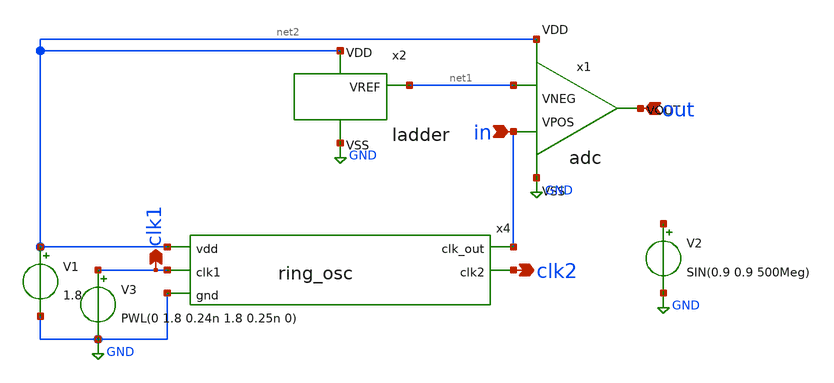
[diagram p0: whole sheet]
** sch_path: week4/xschem/adc/adc_tb.sch
**.subckt adc_tb in out clk1 clk2
*.ipin in
*.ipin out
*.opin clk1
*.opin clk2
x1 out net2 net1 in GND adc
x2 net1 net2 GND ladder
x4 net2 in clk1 clk2 GND ring_osc
V1 net2 GND 1.8
V3 clk1 GND PWL(0 1.8 0.24n 1.8 0.25n 0)
V2 net3 GND SIN(0.9 0.9 500Meg)
**** begin user architecture code


.lib /usr/local/share/pdk/sky130A/libs.tech/ngspice/sky130.lib.spice tt
.control
	tran 0.01n 4n
	plot v(in) v(out)
.endc
.save all


**** end user architecture code
**.ends

* expanding   symbol:  adc.sym # of pins=5
** sym_path: week4/xschem/adc/adc.sym
** sch_path: week4/xschem/adc/adc.sch
.subckt adc VOUT VDD VNEG VPOS VSS
*.ipin VDD
*.opin VOUT
*.ipin VSS
*.ipin VNEG
*.ipin VPOS
XM1 VREF VREF VSS VSS sky130_fd_pr__nfet_01v8 L=0.15 W=1 nf=1 ad='int((nf+1)/2) * W/nf * 0.29' as='int((nf+2)/2) * W/nf * 0.29'
+ pd='2*int((nf+1)/2) * (W/nf + 0.29)' ps='2*int((nf+2)/2) * (W/nf + 0.29)' nrd='0.29 / W' nrs='0.29 / W'
+ sa=0 sb=0 sd=0 mult=1 m=1
XM2 VREF VREF VDD VDD sky130_fd_pr__pfet_01v8 L=0.15 W=1 nf=1 ad='int((nf+1)/2) * W/nf * 0.29' as='int((nf+2)/2) * W/nf * 0.29'
+ pd='2*int((nf+1)/2) * (W/nf + 0.29)' ps='2*int((nf+2)/2) * (W/nf + 0.29)' nrd='0.29 / W' nrs='0.29 / W'
+ sa=0 sb=0 sd=0 mult=1 m=1
XM3 net1 VREF VDD VDD sky130_fd_pr__pfet_01v8 L=0.15 W=3 nf=1 ad='int((nf+1)/2) * W/nf * 0.29' as='int((nf+2)/2) * W/nf * 0.29'
+ pd='2*int((nf+1)/2) * (W/nf + 0.29)' ps='2*int((nf+2)/2) * (W/nf + 0.29)' nrd='0.29 / W' nrs='0.29 / W'
+ sa=0 sb=0 sd=0 mult=1 m=1
XM4 net2 VNEG net1 VDD sky130_fd_pr__pfet_01v8 L=0.15 W=3 nf=1 ad='int((nf+1)/2) * W/nf * 0.29' as='int((nf+2)/2) * W/nf * 0.29'
+ pd='2*int((nf+1)/2) * (W/nf + 0.29)' ps='2*int((nf+2)/2) * (W/nf + 0.29)' nrd='0.29 / W' nrs='0.29 / W'
+ sa=0 sb=0 sd=0 mult=1 m=1
XM5 DIFF VPOS net1 VDD sky130_fd_pr__pfet_01v8 L=0.15 W=3 nf=1 ad='int((nf+1)/2) * W/nf * 0.29' as='int((nf+2)/2) * W/nf * 0.29'
+ pd='2*int((nf+1)/2) * (W/nf + 0.29)' ps='2*int((nf+2)/2) * (W/nf + 0.29)' nrd='0.29 / W' nrs='0.29 / W'
+ sa=0 sb=0 sd=0 mult=1 m=1
XM6 net2 net2 VSS VSS sky130_fd_pr__nfet_01v8 L=0.15 W=1 nf=1 ad='int((nf+1)/2) * W/nf * 0.29' as='int((nf+2)/2) * W/nf * 0.29'
+ pd='2*int((nf+1)/2) * (W/nf + 0.29)' ps='2*int((nf+2)/2) * (W/nf + 0.29)' nrd='0.29 / W' nrs='0.29 / W'
+ sa=0 sb=0 sd=0 mult=1 m=1
XM7 DIFF net2 VSS VSS sky130_fd_pr__nfet_01v8 L=0.15 W=1 nf=1 ad='int((nf+1)/2) * W/nf * 0.29' as='int((nf+2)/2) * W/nf * 0.29'
+ pd='2*int((nf+1)/2) * (W/nf + 0.29)' ps='2*int((nf+2)/2) * (W/nf + 0.29)' nrd='0.29 / W' nrs='0.29 / W'
+ sa=0 sb=0 sd=0 mult=1 m=1
XM8 VOUT DIFF VSS VSS sky130_fd_pr__nfet_01v8 L=0.15 W=1 nf=1 ad='int((nf+1)/2) * W/nf * 0.29' as='int((nf+2)/2) * W/nf * 0.29'
+ pd='2*int((nf+1)/2) * (W/nf + 0.29)' ps='2*int((nf+2)/2) * (W/nf + 0.29)' nrd='0.29 / W' nrs='0.29 / W'
+ sa=0 sb=0 sd=0 mult=1 m=1
XM9 VOUT VREF VDD VDD sky130_fd_pr__pfet_01v8 L=0.15 W=6 nf=1 ad='int((nf+1)/2) * W/nf * 0.29' as='int((nf+2)/2) * W/nf * 0.29'
+ pd='2*int((nf+1)/2) * (W/nf + 0.29)' ps='2*int((nf+2)/2) * (W/nf + 0.29)' nrd='0.29 / W' nrs='0.29 / W'
+ sa=0 sb=0 sd=0 mult=1 m=1
XM10 VOUT DIFF VOUT VSS sky130_fd_pr__nfet_01v8 L=0.15 W=1 nf=1 ad='int((nf+1)/2) * W/nf * 0.29' as='int((nf+2)/2) * W/nf * 0.29'
+ pd='2*int((nf+1)/2) * (W/nf + 0.29)' ps='2*int((nf+2)/2) * (W/nf + 0.29)' nrd='0.29 / W' nrs='0.29 / W'
+ sa=0 sb=0 sd=0 mult=1 m=1
.ends


* expanding   symbol:  ladder.sym # of pins=3
** sym_path: week4/xschem/adc/ladder.sym
** sch_path: week4/xschem/adc/ladder.sch
.subckt ladder VREF VDD VSS
*.opin VREF
*.ipin VSS
*.ipin VDD
XM1 VREF VREF VSS VSS sky130_fd_pr__nfet_01v8 L=0.15 W=1 nf=1 ad='int((nf+1)/2) * W/nf * 0.29' as='int((nf+2)/2) * W/nf * 0.29'
+ pd='2*int((nf+1)/2) * (W/nf + 0.29)' ps='2*int((nf+2)/2) * (W/nf + 0.29)' nrd='0.29 / W' nrs='0.29 / W'
+ sa=0 sb=0 sd=0 mult=1 m=1
XM2 VREF VREF VDD VDD sky130_fd_pr__pfet_01v8 L=0.15 W=1 nf=1 ad='int((nf+1)/2) * W/nf * 0.29' as='int((nf+2)/2) * W/nf * 0.29'
+ pd='2*int((nf+1)/2) * (W/nf + 0.29)' ps='2*int((nf+2)/2) * (W/nf + 0.29)' nrd='0.29 / W' nrs='0.29 / W'
+ sa=0 sb=0 sd=0 mult=1 m=1
.ends


* expanding   symbol:  ring_osc.sym # of pins=5
** sym_path: week4/xschem/ring/ring_osc.sym
** sch_path: week4/xschem/ring/ring_osc.sch
.subckt ring_osc vdd clk_out clk1 clk2 gnd
*.ipin vdd
*.ipin gnd
*.ipin clk1
*.opin clk_out
*.opin clk2
XM7 vdd clk1 net1 gnd sky130_fd_pr__nfet_01v8 L=0.15 W=1 nf=1 ad='int((nf+1)/2) * W/nf * 0.29' as='int((nf+2)/2) * W/nf * 0.29'
+ pd='2*int((nf+1)/2) * (W/nf + 0.29)' ps='2*int((nf+2)/2) * (W/nf + 0.29)' nrd='0.29 / W' nrs='0.29 / W'
+ sa=0 sb=0 sd=0 mult=1 m=1
XM8 clk2 clk1 gnd gnd sky130_fd_pr__nfet_01v8 L=0.15 W=1 nf=1 ad='int((nf+1)/2) * W/nf * 0.29' as='int((nf+2)/2) * W/nf * 0.29'
+ pd='2*int((nf+1)/2) * (W/nf + 0.29)' ps='2*int((nf+2)/2) * (W/nf + 0.29)' nrd='0.29 / W' nrs='0.29 / W'
+ sa=0 sb=0 sd=0 mult=1 m=1
XM9 clk2 clk1 vdd vdd sky130_fd_pr__pfet_01v8 L=0.15 W=1 nf=1 ad='int((nf+1)/2) * W/nf * 0.29' as='int((nf+2)/2) * W/nf * 0.29'
+ pd='2*int((nf+1)/2) * (W/nf + 0.29)' ps='2*int((nf+2)/2) * (W/nf + 0.29)' nrd='0.29 / W' nrs='0.29 / W'
+ sa=0 sb=0 sd=0 mult=1 m=1
XM10 clk_out clk2 net1 gnd sky130_fd_pr__nfet_01v8 L=0.15 W=1 nf=1 ad='int((nf+1)/2) * W/nf * 0.29' as='int((nf+2)/2) * W/nf * 0.29'
+ pd='2*int((nf+1)/2) * (W/nf + 0.29)' ps='2*int((nf+2)/2) * (W/nf + 0.29)' nrd='0.29 / W' nrs='0.29 / W'
+ sa=0 sb=0 sd=0 mult=1 m=1
x1 vdd gnd clk_out net1 sub_comp
.ends


* expanding   symbol:  sub_comp.sym # of pins=4
** sym_path: week4/xschem/ring/sub_comp.sym
** sch_path: week4/xschem/ring/sub_comp.sch
.subckt sub_comp vdd gnd clkout clkin
*.ipin clkin
*.opin clkout
*.ipin vdd
*.ipin gnd
XM1 net1 clkin gnd gnd sky130_fd_pr__nfet_01v8 L=0.15 W=1 nf=1 ad='int((nf+1)/2) * W/nf * 0.29' as='int((nf+2)/2) * W/nf * 0.29'
+ pd='2*int((nf+1)/2) * (W/nf + 0.29)' ps='2*int((nf+2)/2) * (W/nf + 0.29)' nrd='0.29 / W' nrs='0.29 / W'
+ sa=0 sb=0 sd=0 mult=1 m=1
XM2 net1 clkin vdd vdd sky130_fd_pr__pfet_01v8 L=0.15 W=3 nf=1 ad='int((nf+1)/2) * W/nf * 0.29' as='int((nf+2)/2) * W/nf * 0.29'
+ pd='2*int((nf+1)/2) * (W/nf + 0.29)' ps='2*int((nf+2)/2) * (W/nf + 0.29)' nrd='0.29 / W' nrs='0.29 / W'
+ sa=0 sb=0 sd=0 mult=1 m=1
XM3 net2 net1 gnd gnd sky130_fd_pr__nfet_01v8 L=0.15 W=1 nf=1 ad='int((nf+1)/2) * W/nf * 0.29' as='int((nf+2)/2) * W/nf * 0.29'
+ pd='2*int((nf+1)/2) * (W/nf + 0.29)' ps='2*int((nf+2)/2) * (W/nf + 0.29)' nrd='0.29 / W' nrs='0.29 / W'
+ sa=0 sb=0 sd=0 mult=1 m=1
XM4 net2 net1 vdd vdd sky130_fd_pr__pfet_01v8 L=0.15 W=6 nf=1 ad='int((nf+1)/2) * W/nf * 0.29' as='int((nf+2)/2) * W/nf * 0.29'
+ pd='2*int((nf+1)/2) * (W/nf + 0.29)' ps='2*int((nf+2)/2) * (W/nf + 0.29)' nrd='0.29 / W' nrs='0.29 / W'
+ sa=0 sb=0 sd=0 mult=1 m=1
XM7 clkout net3 gnd gnd sky130_fd_pr__nfet_01v8 L=0.15 W=1 nf=1 ad='int((nf+1)/2) * W/nf * 0.29' as='int((nf+2)/2) * W/nf * 0.29'
+ pd='2*int((nf+1)/2) * (W/nf + 0.29)' ps='2*int((nf+2)/2) * (W/nf + 0.29)' nrd='0.29 / W' nrs='0.29 / W'
+ sa=0 sb=0 sd=0 mult=1 m=1
XM8 clkout net3 vdd vdd sky130_fd_pr__pfet_01v8 L=0.15 W=96 nf=2 ad='int((nf+1)/2) * W/nf * 0.29' as='int((nf+2)/2) * W/nf * 0.29'
+ pd='2*int((nf+1)/2) * (W/nf + 0.29)' ps='2*int((nf+2)/2) * (W/nf + 0.29)' nrd='0.29 / W' nrs='0.29 / W'
+ sa=0 sb=0 sd=0 mult=1 m=1
XM5 net4 net2 gnd gnd sky130_fd_pr__nfet_01v8 L=0.15 W=1 nf=1 ad='int((nf+1)/2) * W/nf * 0.29' as='int((nf+2)/2) * W/nf * 0.29'
+ pd='2*int((nf+1)/2) * (W/nf + 0.29)' ps='2*int((nf+2)/2) * (W/nf + 0.29)' nrd='0.29 / W' nrs='0.29 / W'
+ sa=0 sb=0 sd=0 mult=1 m=1
XM6 net4 net2 vdd vdd sky130_fd_pr__pfet_01v8 L=0.15 W=12 nf=1 ad='int((nf+1)/2) * W/nf * 0.29' as='int((nf+2)/2) * W/nf * 0.29'
+ pd='2*int((nf+1)/2) * (W/nf + 0.29)' ps='2*int((nf+2)/2) * (W/nf + 0.29)' nrd='0.29 / W' nrs='0.29 / W'
+ sa=0 sb=0 sd=0 mult=1 m=1
XM9 net5 net4 gnd gnd sky130_fd_pr__nfet_01v8 L=0.15 W=1 nf=1 ad='int((nf+1)/2) * W/nf * 0.29' as='int((nf+2)/2) * W/nf * 0.29'
+ pd='2*int((nf+1)/2) * (W/nf + 0.29)' ps='2*int((nf+2)/2) * (W/nf + 0.29)' nrd='0.29 / W' nrs='0.29 / W'
+ sa=0 sb=0 sd=0 mult=1 m=1
XM10 net5 net4 vdd vdd sky130_fd_pr__pfet_01v8 L=0.15 W=24 nf=1 ad='int((nf+1)/2) * W/nf * 0.29' as='int((nf+2)/2) * W/nf * 0.29'
+ pd='2*int((nf+1)/2) * (W/nf + 0.29)' ps='2*int((nf+2)/2) * (W/nf + 0.29)' nrd='0.29 / W' nrs='0.29 / W'
+ sa=0 sb=0 sd=0 mult=1 m=1
XM11 net6 net5 gnd gnd sky130_fd_pr__nfet_01v8 L=0.15 W=1 nf=1 ad='int((nf+1)/2) * W/nf * 0.29' as='int((nf+2)/2) * W/nf * 0.29'
+ pd='2*int((nf+1)/2) * (W/nf + 0.29)' ps='2*int((nf+2)/2) * (W/nf + 0.29)' nrd='0.29 / W' nrs='0.29 / W'
+ sa=0 sb=0 sd=0 mult=1 m=1
XM12 net6 net5 vdd vdd sky130_fd_pr__pfet_01v8 L=0.15 W=48 nf=1 ad='int((nf+1)/2) * W/nf * 0.29' as='int((nf+2)/2) * W/nf * 0.29'
+ pd='2*int((nf+1)/2) * (W/nf + 0.29)' ps='2*int((nf+2)/2) * (W/nf + 0.29)' nrd='0.29 / W' nrs='0.29 / W'
+ sa=0 sb=0 sd=0 mult=1 m=1
XM13 net3 net6 gnd gnd sky130_fd_pr__nfet_01v8 L=0.15 W=1 nf=1 ad='int((nf+1)/2) * W/nf * 0.29' as='int((nf+2)/2) * W/nf * 0.29'
+ pd='2*int((nf+1)/2) * (W/nf + 0.29)' ps='2*int((nf+2)/2) * (W/nf + 0.29)' nrd='0.29 / W' nrs='0.29 / W'
+ sa=0 sb=0 sd=0 mult=1 m=1
XM14 net3 net6 vdd vdd sky130_fd_pr__pfet_01v8 L=0.15 W=96 nf=1 ad='int((nf+1)/2) * W/nf * 0.29' as='int((nf+2)/2) * W/nf * 0.29'
+ pd='2*int((nf+1)/2) * (W/nf + 0.29)' ps='2*int((nf+2)/2) * (W/nf + 0.29)' nrd='0.29 / W' nrs='0.29 / W'
+ sa=0 sb=0 sd=0 mult=1 m=1
.ends

.GLOBAL GND
.end
